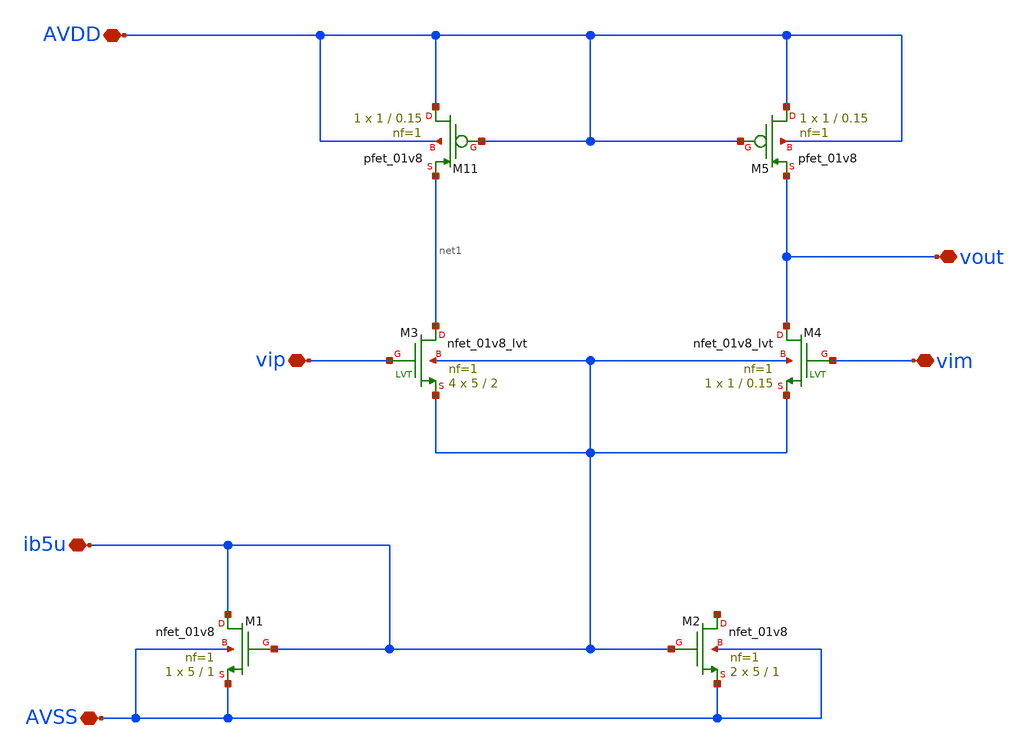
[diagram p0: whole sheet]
** sch_path: xschem/opa_nmos1.sch
**.subckt opa_nmos1 vip vim vout ib5u AVDD AVSS
*.iopin vip
*.iopin vim
*.iopin vout
*.iopin ib5u
*.iopin AVDD
*.iopin AVSS
XM1 ib5u ib5u AVSS AVSS sky130_fd_pr__nfet_01v8 L=1 W=5 nf=1 ad='int((1 + 1)/2) * 5 / 1 * 0.29' as='int((1 + 2)/2) * 5 / 1 * 0.29'
+ pd='2*int((1 + 1)/2) * (5 / 1 + 0.29)' ps='2*int((1 + 2)/2) * (5 / 1 + 0.29)' nrd='0.29 / 5 ' nrs='0.29 / 5 '
+ sa=0 sb=0 sd=0 mult=1 m=1
XM2 net2 ib5u AVSS AVSS sky130_fd_pr__nfet_01v8 L=1 W=5 nf=1 ad='int((1 + 1)/2) * 5 / 1 * 0.29' as='int((1 + 2)/2) * 5 / 1 * 0.29'
+ pd='2*int((1 + 1)/2) * (5 / 1 + 0.29)' ps='2*int((1 + 2)/2) * (5 / 1 + 0.29)' nrd='0.29 / 5 ' nrs='0.29 / 5 '
+ sa=0 sb=0 sd=0 mult=2 m=2
XM3 net1 vip ib5u ib5u sky130_fd_pr__nfet_01v8_lvt L=2 W=5 nf=1 ad='int((1 + 1)/2) * 5 / 1 * 0.29' as='int((1 + 2)/2) * 5 / 1 * 0.29'
+ pd='2*int((1 + 1)/2) * (5 / 1 + 0.29)' ps='2*int((1 + 2)/2) * (5 / 1 + 0.29)' nrd='0.29 / 5 ' nrs='0.29 / 5 '
+ sa=0 sb=0 sd=0 mult=4 m=4
XM4 vout vim ib5u ib5u sky130_fd_pr__nfet_01v8_lvt L=0.15 W=1 nf=1 ad='int((1 + 1)/2) * 1 / 1 * 0.29'
+ as='int((1 + 2)/2) * 1 / 1 * 0.29' pd='2*int((1 + 1)/2) * (1 / 1 + 0.29)' ps='2*int((1 + 2)/2) * (1 / 1 + 0.29)'
+ nrd='0.29 / 1 ' nrs='0.29 / 1 ' sa=0 sb=0 sd=0 mult=1 m=1
XM11 AVDD AVDD net1 AVDD sky130_fd_pr__pfet_01v8 L=0.15 W=1 nf=1 ad='int((nf+1)/2) * W/nf * 0.29' as='int((nf+2)/2) * W/nf * 0.29'
+ pd='2*int((nf+1)/2) * (W/nf + 0.29)' ps='2*int((nf+2)/2) * (W/nf + 0.29)' nrd='0.29 / W' nrs='0.29 / W'
+ sa=0 sb=0 sd=0 mult=1 m=1
XM5 AVDD AVDD vout AVDD sky130_fd_pr__pfet_01v8 L=0.15 W=1 nf=1 ad='int((nf+1)/2) * W/nf * 0.29' as='int((nf+2)/2) * W/nf * 0.29'
+ pd='2*int((nf+1)/2) * (W/nf + 0.29)' ps='2*int((nf+2)/2) * (W/nf + 0.29)' nrd='0.29 / W' nrs='0.29 / W'
+ sa=0 sb=0 sd=0 mult=1 m=1
**.ends
.end
